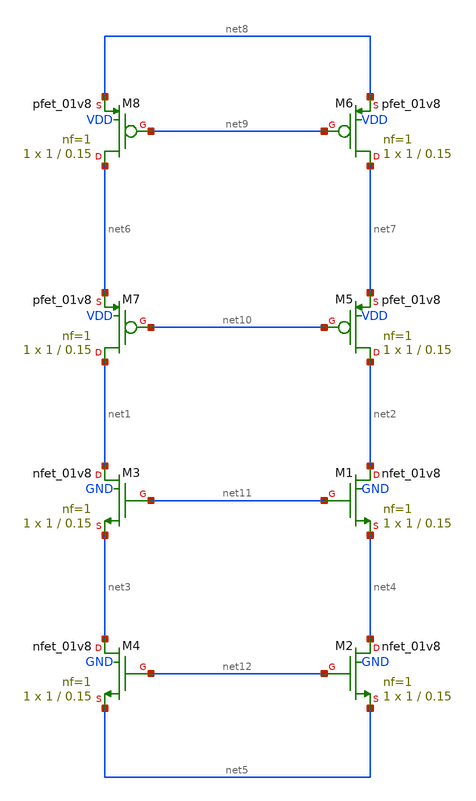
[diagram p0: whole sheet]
** sch_path: xschem/Amplifiers/Rail2RailTwostage.sch
**.subckt Rail2RailTwostage
XM1 net2 net11 net4 GND sky130_fd_pr__nfet_01v8 L=0.15 W=1 nf=1 ad='int((nf+1)/2) * W/nf * 0.29' as='int((nf+2)/2) * W/nf * 0.29'
+ pd='2*int((nf+1)/2) * (W/nf + 0.29)' ps='2*int((nf+2)/2) * (W/nf + 0.29)' nrd='0.29 / W' nrs='0.29 / W'
+ sa=0 sb=0 sd=0 mult=1 m=1
XM2 net4 net12 net5 GND sky130_fd_pr__nfet_01v8 L=0.15 W=1 nf=1 ad='int((nf+1)/2) * W/nf * 0.29' as='int((nf+2)/2) * W/nf * 0.29'
+ pd='2*int((nf+1)/2) * (W/nf + 0.29)' ps='2*int((nf+2)/2) * (W/nf + 0.29)' nrd='0.29 / W' nrs='0.29 / W'
+ sa=0 sb=0 sd=0 mult=1 m=1
XM3 net1 net11 net3 GND sky130_fd_pr__nfet_01v8 L=0.15 W=1 nf=1 ad='int((nf+1)/2) * W/nf * 0.29' as='int((nf+2)/2) * W/nf * 0.29'
+ pd='2*int((nf+1)/2) * (W/nf + 0.29)' ps='2*int((nf+2)/2) * (W/nf + 0.29)' nrd='0.29 / W' nrs='0.29 / W'
+ sa=0 sb=0 sd=0 mult=1 m=1
XM4 net3 net12 net5 GND sky130_fd_pr__nfet_01v8 L=0.15 W=1 nf=1 ad='int((nf+1)/2) * W/nf * 0.29' as='int((nf+2)/2) * W/nf * 0.29'
+ pd='2*int((nf+1)/2) * (W/nf + 0.29)' ps='2*int((nf+2)/2) * (W/nf + 0.29)' nrd='0.29 / W' nrs='0.29 / W'
+ sa=0 sb=0 sd=0 mult=1 m=1
XM5 net2 net10 net7 VDD sky130_fd_pr__pfet_01v8 L=0.15 W=1 nf=1 ad='int((nf+1)/2) * W/nf * 0.29' as='int((nf+2)/2) * W/nf * 0.29'
+ pd='2*int((nf+1)/2) * (W/nf + 0.29)' ps='2*int((nf+2)/2) * (W/nf + 0.29)' nrd='0.29 / W' nrs='0.29 / W'
+ sa=0 sb=0 sd=0 mult=1 m=1
XM6 net7 net9 net8 VDD sky130_fd_pr__pfet_01v8 L=0.15 W=1 nf=1 ad='int((nf+1)/2) * W/nf * 0.29' as='int((nf+2)/2) * W/nf * 0.29'
+ pd='2*int((nf+1)/2) * (W/nf + 0.29)' ps='2*int((nf+2)/2) * (W/nf + 0.29)' nrd='0.29 / W' nrs='0.29 / W'
+ sa=0 sb=0 sd=0 mult=1 m=1
XM7 net1 net10 net6 VDD sky130_fd_pr__pfet_01v8 L=0.15 W=1 nf=1 ad='int((nf+1)/2) * W/nf * 0.29' as='int((nf+2)/2) * W/nf * 0.29'
+ pd='2*int((nf+1)/2) * (W/nf + 0.29)' ps='2*int((nf+2)/2) * (W/nf + 0.29)' nrd='0.29 / W' nrs='0.29 / W'
+ sa=0 sb=0 sd=0 mult=1 m=1
XM8 net6 net9 net8 VDD sky130_fd_pr__pfet_01v8 L=0.15 W=1 nf=1 ad='int((nf+1)/2) * W/nf * 0.29' as='int((nf+2)/2) * W/nf * 0.29'
+ pd='2*int((nf+1)/2) * (W/nf + 0.29)' ps='2*int((nf+2)/2) * (W/nf + 0.29)' nrd='0.29 / W' nrs='0.29 / W'
+ sa=0 sb=0 sd=0 mult=1 m=1
**.ends
.end
